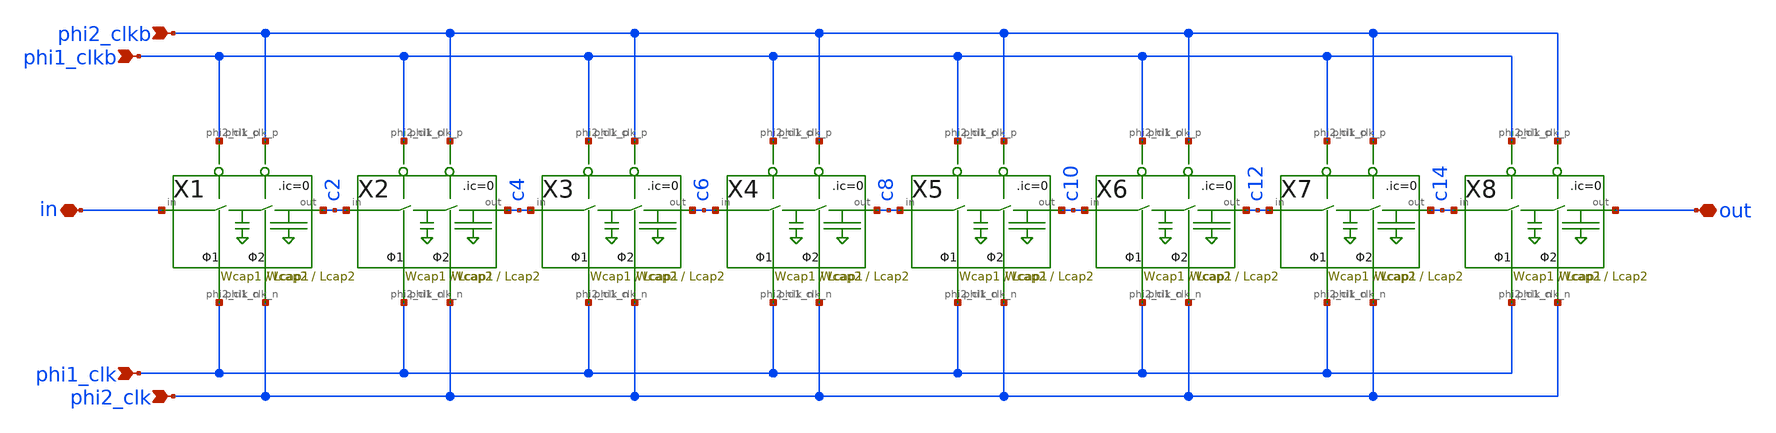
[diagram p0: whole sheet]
** sch_path: xschem/Switched_Caps/16switchcaps_2phi.sch
**.subckt 16switchcaps_2phi in out phi2_clkb phi1_clkb phi2_clk phi1_clk
*.iopin in
*.iopin out
*.ipin phi2_clkb
*.ipin phi1_clkb
*.ipin phi2_clk
*.ipin phi1_clk
X1 in c2 phi2_clk phi1_clk phi1_clkb phi2_clkb 2switchcaps Wcap1=Wcap1 Lcap1=Lcap1 Wcap2=Wcap2
+ Lcap2=Lcap2
X2 c2 c4 phi2_clk phi1_clk phi1_clkb phi2_clkb 2switchcaps Wcap1=Wcap1 Lcap1=Lcap1 Wcap2=Wcap2
+ Lcap2=Lcap2
X3 c4 c6 phi2_clk phi1_clk phi1_clkb phi2_clkb 2switchcaps Wcap1=Wcap1 Lcap1=Lcap1 Wcap2=Wcap2
+ Lcap2=Lcap2
X4 c6 c8 phi2_clk phi1_clk phi1_clkb phi2_clkb 2switchcaps Wcap1=Wcap1 Lcap1=Lcap1 Wcap2=Wcap2
+ Lcap2=Lcap2
X5 c8 c10 phi2_clk phi1_clk phi1_clkb phi2_clkb 2switchcaps Wcap1=Wcap1 Lcap1=Lcap1 Wcap2=Wcap2
+ Lcap2=Lcap2
X6 c10 c12 phi2_clk phi1_clk phi1_clkb phi2_clkb 2switchcaps Wcap1=Wcap1 Lcap1=Lcap1 Wcap2=Wcap2
+ Lcap2=Lcap2
X7 c12 c14 phi2_clk phi1_clk phi1_clkb phi2_clkb 2switchcaps Wcap1=Wcap1 Lcap1=Lcap1 Wcap2=Wcap2
+ Lcap2=Lcap2
X8 c14 out phi2_clk phi1_clk phi1_clkb phi2_clkb 2switchcaps Wcap1=Wcap1 Lcap1=Lcap1 Wcap2=Wcap2
+ Lcap2=Lcap2
**.ends

* expanding   symbol:  Switched_Caps/2switchcaps.sym # of pins=6
** sym_path: xschem/Switched_Caps/2switchcaps.sym
** sch_path: xschem/Switched_Caps/2switchcaps.sch
.subckt 2switchcaps in out phi2_clk_n phi1_clk_n phi1_clk_p phi2_clk_p  Wcap1=4 Lcap1=2.5 Wcap2=4
+ Lcap2=25
*.iopin out
*.iopin in
*.ipin phi1_clk_n
*.ipin phi1_clk_p
*.ipin phi2_clk_p
*.ipin phi2_clk_n
XC1 c1 GND sky130_fd_pr__cap_mim_m3_1 W=Wcap1 L=Lcap1 MF=1 m=1
XC2 out GND sky130_fd_pr__cap_mim_m3_1 W=Wcap2 L=Lcap2 MF=1 m=1
**** begin user architecture code

.ic v(c1)=0 v(out)=0

**** end user architecture code
X1 in c1 phi1_clk_p phi1_clk_n transmission_gate Wpmos=0.42 Lpmos=0.18 Wnmos=0.42 Lnmos=0.18
X2 c1 out phi2_clk_p phi2_clk_n transmission_gate Wpmos=0.42 Lpmos=0.18 Wnmos=0.42 Lnmos=0.18
.ends


* expanding   symbol:  transmission_gate/transmission_gate.sym # of pins=4
** sym_path: xschem/transmission_gate/transmission_gate.sym
** sch_path: xschem/transmission_gate/transmission_gate.sch
.subckt transmission_gate in out ctrl_ ctrl  Wpmos=0.42 Lpmos=0.18 Wnmos=0.42 Lnmos=0.18
*.iopin in
*.iopin out
*.ipin ctrl_
*.ipin ctrl
XM1 out ctrl in GND sky130_fd_pr__nfet_01v8 L=Lnmos W=Wnmos nf=1 ad='int((nf+1)/2) * W/nf * 0.29' as='int((nf+2)/2) * W/nf * 0.29'
+ pd='2*int((nf+1)/2) * (W/nf + 0.29)' ps='2*int((nf+2)/2) * (W/nf + 0.29)' nrd='0.29 / W' nrs='0.29 / W'
+ sa=0 sb=0 sd=0 mult=1 m=1
XM2 out ctrl_ in VDD sky130_fd_pr__pfet_01v8 L=Lpmos W=Wpmos nf=1 ad='int((nf+1)/2) * W/nf * 0.29' as='int((nf+2)/2) * W/nf * 0.29'
+ pd='2*int((nf+1)/2) * (W/nf + 0.29)' ps='2*int((nf+2)/2) * (W/nf + 0.29)' nrd='0.29 / W' nrs='0.29 / W'
+ sa=0 sb=0 sd=0 mult=1 m=1
.ends

.GLOBAL GND
.GLOBAL VDD
.end
